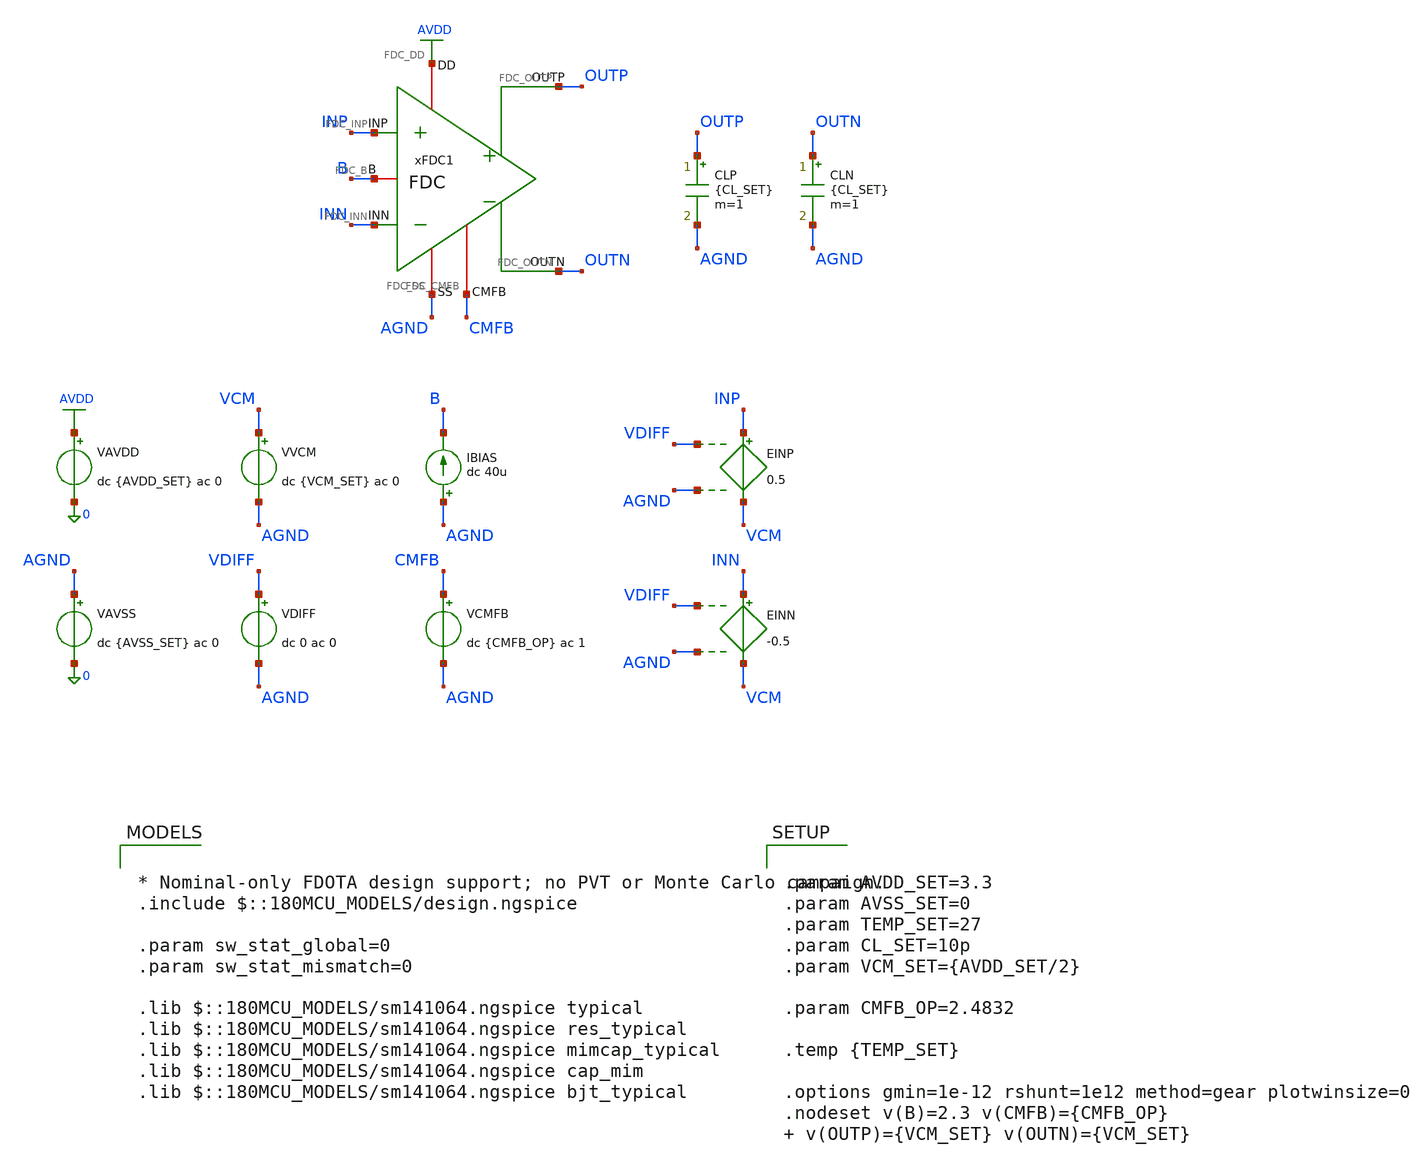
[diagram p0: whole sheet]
** sch_path: Design_Files/IC Design/Testbench/ANALOG_BLOCKS/FDOTA/FDC/FDC_TB_CM_PLANT.sch
**.subckt FDC_TB_CM_PLANT
IBIAS AGND B dc 40u
VAVDD AVDD 0 dc {AVDD_SET} ac 0
.save i(vavdd)
CLP OUTP AGND {CL_SET} m=1
VVCM VCM AGND dc {VCM_SET} ac 0
VDIFF VDIFF AGND dc 0 ac 0
VAVSS AGND 0 dc {AVSS_SET} ac 0
.save i(vavss)
EINN INN VCM VDIFF AGND -0.5
EINP INP VCM VDIFF AGND 0.5
CLN OUTN AGND {CL_SET} m=1
VCMFB CMFB AGND dc {CMFB_OP} ac 1
xFDC1 AVDD AGND INP INN OUTN B OUTP CMFB FDC
**** begin user architecture code

* Nominal-only FDOTA design support; no PVT or Monte Carlo campaign.
.include $::180MCU_MODELS/design.ngspice

.param sw_stat_global=0
.param sw_stat_mismatch=0

.lib $::180MCU_MODELS/sm141064.ngspice typical
.lib $::180MCU_MODELS/sm141064.ngspice res_typical
.lib $::180MCU_MODELS/sm141064.ngspice mimcap_typical
.lib $::180MCU_MODELS/sm141064.ngspice cap_mim
.lib $::180MCU_MODELS/sm141064.ngspice bjt_typical




.control
destroy all
save all
set noaskquit
set wr_vecnames
set wr_singlescale
option numdgt=15

shell mkdir -p
+ /foss/designs/ECG_Acquisition_IC/Measurement_Results/IC_Simulation/ANALOG_BLOCKS/FDOTA/FDC/Result_txt

shell rm -f
+ /foss/designs/ECG_Acquisition_IC/Measurement_Results/IC_Simulation/ANALOG_BLOCKS/FDOTA/FDC/Result_txt/plant_ac.txt

alter @VAVDD[ACMAG]  = 0
alter @VAVSS[ACMAG]  = 0
alter @VVCM[ACMAG]   = 0
alter @VDIFF[ACMAG]  = 0

alter @VCMFB[ACMAG]   = 1
alter @VCMFB[ACPHASE] = 0

ac dec 200 0.1 1G

let vcmfb_ac  = v(cmfb)-v(agnd)
let voutp_ac  = v(outp)-v(agnd)
let voutn_ac  = v(outn)-v(agnd)
let voutcm_ac = (voutp_ac+voutn_ac)/2

let plant_ac   = voutcm_ac/vcmfb_ac
let plant_real = real(plant_ac)
let plant_imag = imag(plant_ac)

setscale frequency

wrdata
+ /foss/designs/ECG_Acquisition_IC/Measurement_Results/IC_Simulation/ANALOG_BLOCKS/FDOTA/FDC/Result_txt/plant_ac.txt plant_real plant_imag

quit
.endc




.param AVDD_SET=3.3
.param AVSS_SET=0
.param TEMP_SET=27
.param CL_SET=10p
.param VCM_SET={AVDD_SET/2}

.param CMFB_OP=2.4832

.temp {TEMP_SET}

.options gmin=1e-12 rshunt=1e12 method=gear plotwinsize=0
.nodeset v(B)=2.3 v(CMFB)={CMFB_OP}  v(OUTP)={VCM_SET} v(OUTN)={VCM_SET}


**** end user architecture code
**.ends
.GLOBAL AVDD
.end
